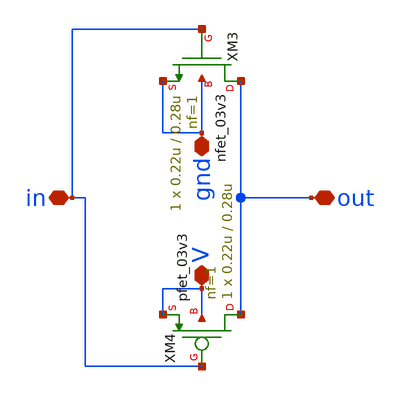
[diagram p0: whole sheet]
** sch_path: xschem/inv_gate.sch
**.subckt inv_gate in out gnd V
*.iopin in
*.iopin out
*.iopin gnd
*.iopin V
XM3 out in gnd gnd nfet_03v3 L=0.28u W=0.22u nf=1 ad='int((nf+1)/2) * W/nf * 0.18u' as='int((nf+2)/2) * W/nf * 0.18u'
+ pd='2*int((nf+1)/2) * (W/nf + 0.18u)' ps='2*int((nf+2)/2) * (W/nf + 0.18u)' nrd='0.18u / W' nrs='0.18u / W'
+ sa=0 sb=0 sd=0 m=1
XM4 out in V V pfet_03v3 L=0.28u W=0.22u nf=1 ad='int((nf+1)/2) * W/nf * 0.18u' as='int((nf+2)/2) * W/nf * 0.18u'
+ pd='2*int((nf+1)/2) * (W/nf + 0.18u)' ps='2*int((nf+2)/2) * (W/nf + 0.18u)' nrd='0.18u / W' nrs='0.18u / W'
+ sa=0 sb=0 sd=0 m=1
**.ends
.end
